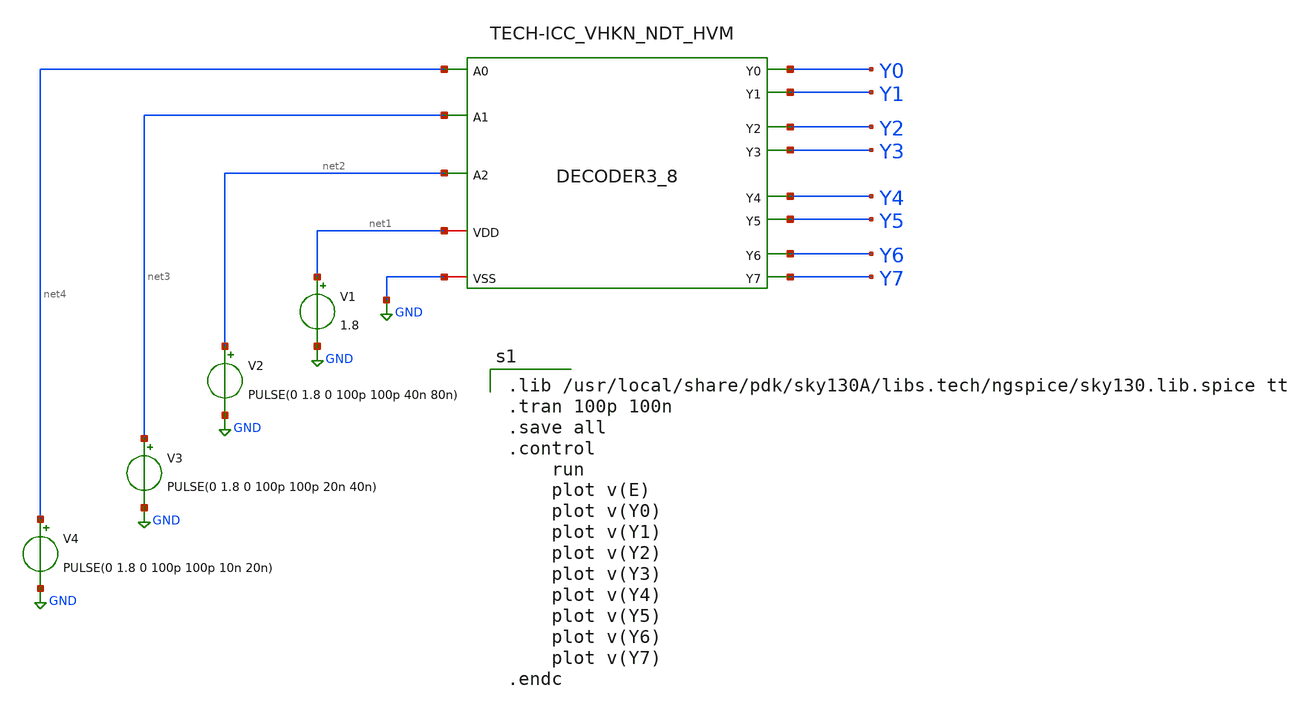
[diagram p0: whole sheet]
** sch_path: DECODER3TO8/Schematic/CMOS_DECODER3_8.sch
**.subckt CMOS_DECODER3_8
x1 net4 Y0 net3 Y1 Y2 net1 Y3 GND Y4 Y5 Y6 Y7 net2 DECODER3_8
V1 net1 GND 1.8
V2 net2 GND PULSE(0 1.8 0 100p 100p 40n 80n)
V3 net3 GND PULSE(0 1.8 0 100p 100p 20n 40n)
V4 net4 GND PULSE(0 1.8 0 100p 100p 10n 20n)
**** begin user architecture code

.lib /usr/local/share/pdk/sky130A/libs.tech/ngspice/sky130.lib.spice tt
.tran 100p 100n
.save all
.control
    run
    plot v(E)
    plot v(Y0)
    plot v(Y1)
    plot v(Y2)
    plot v(Y3)
    plot v(Y4)
    plot v(Y5)
    plot v(Y6)
    plot v(Y7)
.endc


**** end user architecture code
**.ends
.GLOBAL GND
.end
